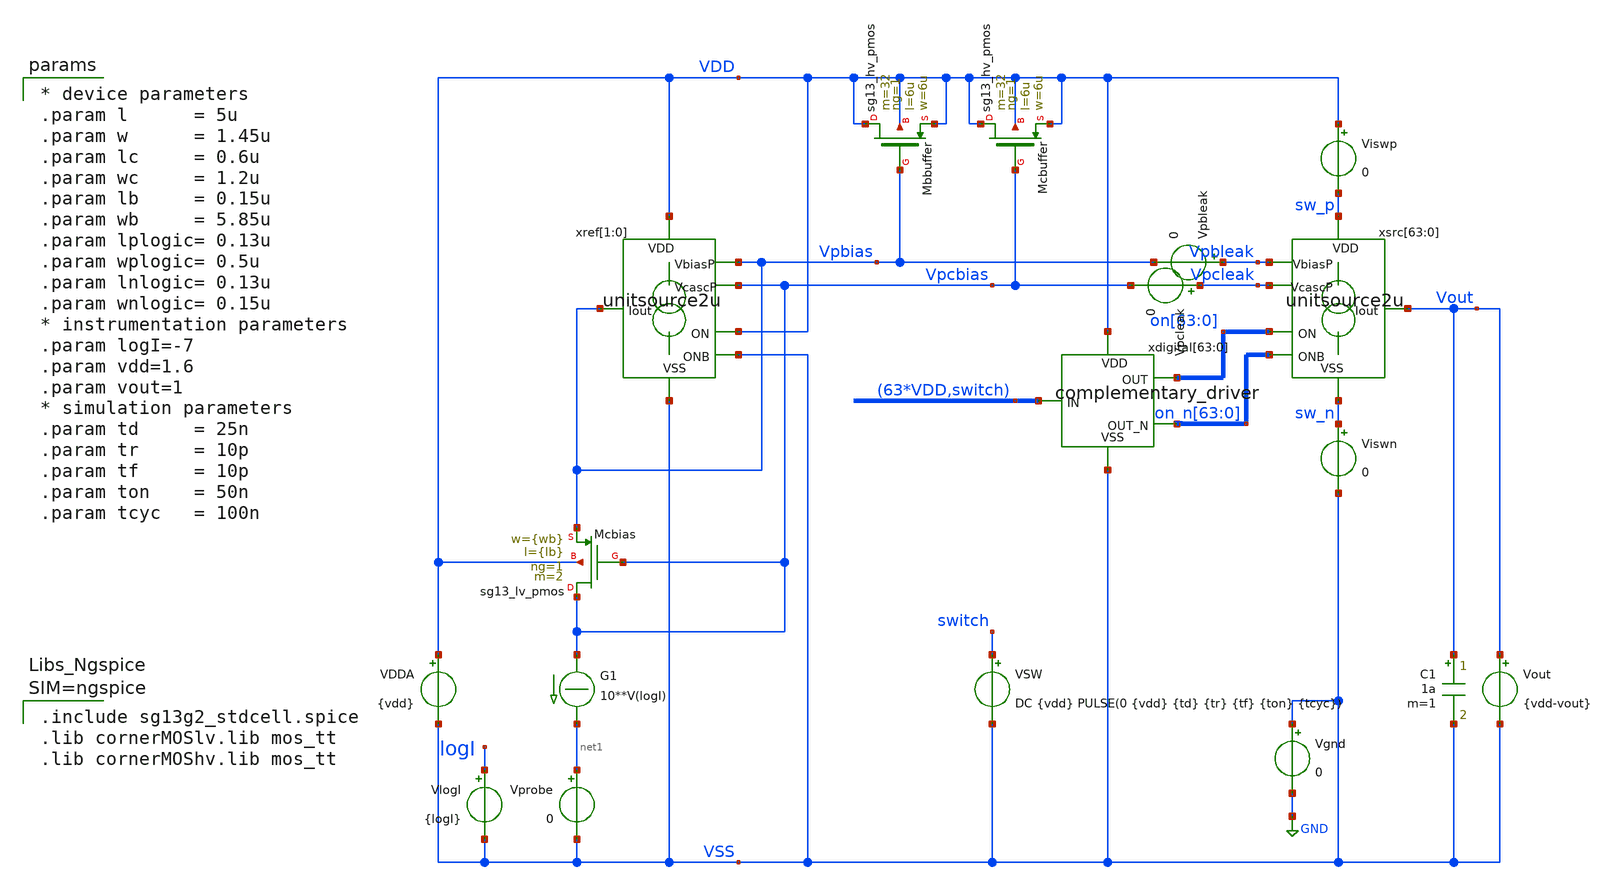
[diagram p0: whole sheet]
** sch_path: xschem/test_unitsource2u_tran.sch
**.subckt test_unitsource2u_tran
Vout Vout VSS {vdd-vout}
.save i(vout)
Vprobe net1 VSS 0
.save i(vprobe)
G1 Vpcbias net1 CUR=' 10**V(logI) '
VlogI logI VSS {logI}
.save i(vlogi)
VDDA VDD VSS {vdd}
.save i(vdda)
XMcbias Vpcbias Vpcbias Vpbias VDD sg13_lv_pmos w={wb} l={lb} ng=1 m=2 mm_ok=1
VSW switch VSS DC {vdd} PULSE(0 {vdd} {td} {tr} {tf} {ton} {tcyc})
.save i(vsw)
XMcbuffer VDD Vpcbias VDD VDD sg13_hv_pmos w=6u l=6u ng=1 m=32 mm_ok=1
XMbbuffer VDD Vpbias VDD VDD sg13_hv_pmos w=6u l=6u ng=1 m=32 mm_ok=1
xref[1] VDD Vpbias VDD VSS Vpbias Vpcbias VSS unitsource2u
xref[0] VDD Vpbias VDD VSS Vpbias Vpcbias VSS unitsource2u
xsrc[63] sw_p Vpbleak on[63] on_n[63] Vout Vpcleak sw_n unitsource2u
xsrc[62] sw_p Vpbleak on[62] on_n[62] Vout Vpcleak sw_n unitsource2u
xsrc[61] sw_p Vpbleak on[61] on_n[61] Vout Vpcleak sw_n unitsource2u
xsrc[60] sw_p Vpbleak on[60] on_n[60] Vout Vpcleak sw_n unitsource2u
xsrc[59] sw_p Vpbleak on[59] on_n[59] Vout Vpcleak sw_n unitsource2u
xsrc[58] sw_p Vpbleak on[58] on_n[58] Vout Vpcleak sw_n unitsource2u
xsrc[57] sw_p Vpbleak on[57] on_n[57] Vout Vpcleak sw_n unitsource2u
xsrc[56] sw_p Vpbleak on[56] on_n[56] Vout Vpcleak sw_n unitsource2u
xsrc[55] sw_p Vpbleak on[55] on_n[55] Vout Vpcleak sw_n unitsource2u
xsrc[54] sw_p Vpbleak on[54] on_n[54] Vout Vpcleak sw_n unitsource2u
xsrc[53] sw_p Vpbleak on[53] on_n[53] Vout Vpcleak sw_n unitsource2u
xsrc[52] sw_p Vpbleak on[52] on_n[52] Vout Vpcleak sw_n unitsource2u
xsrc[51] sw_p Vpbleak on[51] on_n[51] Vout Vpcleak sw_n unitsource2u
xsrc[50] sw_p Vpbleak on[50] on_n[50] Vout Vpcleak sw_n unitsource2u
xsrc[49] sw_p Vpbleak on[49] on_n[49] Vout Vpcleak sw_n unitsource2u
xsrc[48] sw_p Vpbleak on[48] on_n[48] Vout Vpcleak sw_n unitsource2u
xsrc[47] sw_p Vpbleak on[47] on_n[47] Vout Vpcleak sw_n unitsource2u
xsrc[46] sw_p Vpbleak on[46] on_n[46] Vout Vpcleak sw_n unitsource2u
xsrc[45] sw_p Vpbleak on[45] on_n[45] Vout Vpcleak sw_n unitsource2u
xsrc[44] sw_p Vpbleak on[44] on_n[44] Vout Vpcleak sw_n unitsource2u
xsrc[43] sw_p Vpbleak on[43] on_n[43] Vout Vpcleak sw_n unitsource2u
xsrc[42] sw_p Vpbleak on[42] on_n[42] Vout Vpcleak sw_n unitsource2u
xsrc[41] sw_p Vpbleak on[41] on_n[41] Vout Vpcleak sw_n unitsource2u
xsrc[40] sw_p Vpbleak on[40] on_n[40] Vout Vpcleak sw_n unitsource2u
xsrc[39] sw_p Vpbleak on[39] on_n[39] Vout Vpcleak sw_n unitsource2u
xsrc[38] sw_p Vpbleak on[38] on_n[38] Vout Vpcleak sw_n unitsource2u
xsrc[37] sw_p Vpbleak on[37] on_n[37] Vout Vpcleak sw_n unitsource2u
xsrc[36] sw_p Vpbleak on[36] on_n[36] Vout Vpcleak sw_n unitsource2u
xsrc[35] sw_p Vpbleak on[35] on_n[35] Vout Vpcleak sw_n unitsource2u
xsrc[34] sw_p Vpbleak on[34] on_n[34] Vout Vpcleak sw_n unitsource2u
xsrc[33] sw_p Vpbleak on[33] on_n[33] Vout Vpcleak sw_n unitsource2u
xsrc[32] sw_p Vpbleak on[32] on_n[32] Vout Vpcleak sw_n unitsource2u
xsrc[31] sw_p Vpbleak on[31] on_n[31] Vout Vpcleak sw_n unitsource2u
xsrc[30] sw_p Vpbleak on[30] on_n[30] Vout Vpcleak sw_n unitsource2u
xsrc[29] sw_p Vpbleak on[29] on_n[29] Vout Vpcleak sw_n unitsource2u
xsrc[28] sw_p Vpbleak on[28] on_n[28] Vout Vpcleak sw_n unitsource2u
xsrc[27] sw_p Vpbleak on[27] on_n[27] Vout Vpcleak sw_n unitsource2u
xsrc[26] sw_p Vpbleak on[26] on_n[26] Vout Vpcleak sw_n unitsource2u
xsrc[25] sw_p Vpbleak on[25] on_n[25] Vout Vpcleak sw_n unitsource2u
xsrc[24] sw_p Vpbleak on[24] on_n[24] Vout Vpcleak sw_n unitsource2u
xsrc[23] sw_p Vpbleak on[23] on_n[23] Vout Vpcleak sw_n unitsource2u
xsrc[22] sw_p Vpbleak on[22] on_n[22] Vout Vpcleak sw_n unitsource2u
xsrc[21] sw_p Vpbleak on[21] on_n[21] Vout Vpcleak sw_n unitsource2u
xsrc[20] sw_p Vpbleak on[20] on_n[20] Vout Vpcleak sw_n unitsource2u
xsrc[19] sw_p Vpbleak on[19] on_n[19] Vout Vpcleak sw_n unitsource2u
xsrc[18] sw_p Vpbleak on[18] on_n[18] Vout Vpcleak sw_n unitsource2u
xsrc[17] sw_p Vpbleak on[17] on_n[17] Vout Vpcleak sw_n unitsource2u
xsrc[16] sw_p Vpbleak on[16] on_n[16] Vout Vpcleak sw_n unitsource2u
xsrc[15] sw_p Vpbleak on[15] on_n[15] Vout Vpcleak sw_n unitsource2u
xsrc[14] sw_p Vpbleak on[14] on_n[14] Vout Vpcleak sw_n unitsource2u
xsrc[13] sw_p Vpbleak on[13] on_n[13] Vout Vpcleak sw_n unitsource2u
xsrc[12] sw_p Vpbleak on[12] on_n[12] Vout Vpcleak sw_n unitsource2u
xsrc[11] sw_p Vpbleak on[11] on_n[11] Vout Vpcleak sw_n unitsource2u
xsrc[10] sw_p Vpbleak on[10] on_n[10] Vout Vpcleak sw_n unitsource2u
xsrc[9] sw_p Vpbleak on[9] on_n[9] Vout Vpcleak sw_n unitsource2u
xsrc[8] sw_p Vpbleak on[8] on_n[8] Vout Vpcleak sw_n unitsource2u
xsrc[7] sw_p Vpbleak on[7] on_n[7] Vout Vpcleak sw_n unitsource2u
xsrc[6] sw_p Vpbleak on[6] on_n[6] Vout Vpcleak sw_n unitsource2u
xsrc[5] sw_p Vpbleak on[5] on_n[5] Vout Vpcleak sw_n unitsource2u
xsrc[4] sw_p Vpbleak on[4] on_n[4] Vout Vpcleak sw_n unitsource2u
xsrc[3] sw_p Vpbleak on[3] on_n[3] Vout Vpcleak sw_n unitsource2u
xsrc[2] sw_p Vpbleak on[2] on_n[2] Vout Vpcleak sw_n unitsource2u
xsrc[1] sw_p Vpbleak on[1] on_n[1] Vout Vpcleak sw_n unitsource2u
xsrc[0] sw_p Vpbleak on[0] on_n[0] Vout Vpcleak sw_n unitsource2u
Viswp VDD sw_p 0
.save i(viswp)
Viswn sw_n VSS 0
.save i(viswn)
C1 Vout VSS 1a m=1
Vgnd VSS GND 0
.save i(vgnd)
xdigital[63] VDD on[63] VDD on_n[63] VSS complementary_driver
xdigital[62] VDD on[62] VDD on_n[62] VSS complementary_driver
xdigital[61] VDD on[61] VDD on_n[61] VSS complementary_driver
xdigital[60] VDD on[60] VDD on_n[60] VSS complementary_driver
xdigital[59] VDD on[59] VDD on_n[59] VSS complementary_driver
xdigital[58] VDD on[58] VDD on_n[58] VSS complementary_driver
xdigital[57] VDD on[57] VDD on_n[57] VSS complementary_driver
xdigital[56] VDD on[56] VDD on_n[56] VSS complementary_driver
xdigital[55] VDD on[55] VDD on_n[55] VSS complementary_driver
xdigital[54] VDD on[54] VDD on_n[54] VSS complementary_driver
xdigital[53] VDD on[53] VDD on_n[53] VSS complementary_driver
xdigital[52] VDD on[52] VDD on_n[52] VSS complementary_driver
xdigital[51] VDD on[51] VDD on_n[51] VSS complementary_driver
xdigital[50] VDD on[50] VDD on_n[50] VSS complementary_driver
xdigital[49] VDD on[49] VDD on_n[49] VSS complementary_driver
xdigital[48] VDD on[48] VDD on_n[48] VSS complementary_driver
xdigital[47] VDD on[47] VDD on_n[47] VSS complementary_driver
xdigital[46] VDD on[46] VDD on_n[46] VSS complementary_driver
xdigital[45] VDD on[45] VDD on_n[45] VSS complementary_driver
xdigital[44] VDD on[44] VDD on_n[44] VSS complementary_driver
xdigital[43] VDD on[43] VDD on_n[43] VSS complementary_driver
xdigital[42] VDD on[42] VDD on_n[42] VSS complementary_driver
xdigital[41] VDD on[41] VDD on_n[41] VSS complementary_driver
xdigital[40] VDD on[40] VDD on_n[40] VSS complementary_driver
xdigital[39] VDD on[39] VDD on_n[39] VSS complementary_driver
xdigital[38] VDD on[38] VDD on_n[38] VSS complementary_driver
xdigital[37] VDD on[37] VDD on_n[37] VSS complementary_driver
xdigital[36] VDD on[36] VDD on_n[36] VSS complementary_driver
xdigital[35] VDD on[35] VDD on_n[35] VSS complementary_driver
xdigital[34] VDD on[34] VDD on_n[34] VSS complementary_driver
xdigital[33] VDD on[33] VDD on_n[33] VSS complementary_driver
xdigital[32] VDD on[32] VDD on_n[32] VSS complementary_driver
xdigital[31] VDD on[31] VDD on_n[31] VSS complementary_driver
xdigital[30] VDD on[30] VDD on_n[30] VSS complementary_driver
xdigital[29] VDD on[29] VDD on_n[29] VSS complementary_driver
xdigital[28] VDD on[28] VDD on_n[28] VSS complementary_driver
xdigital[27] VDD on[27] VDD on_n[27] VSS complementary_driver
xdigital[26] VDD on[26] VDD on_n[26] VSS complementary_driver
xdigital[25] VDD on[25] VDD on_n[25] VSS complementary_driver
xdigital[24] VDD on[24] VDD on_n[24] VSS complementary_driver
xdigital[23] VDD on[23] VDD on_n[23] VSS complementary_driver
xdigital[22] VDD on[22] VDD on_n[22] VSS complementary_driver
xdigital[21] VDD on[21] VDD on_n[21] VSS complementary_driver
xdigital[20] VDD on[20] VDD on_n[20] VSS complementary_driver
xdigital[19] VDD on[19] VDD on_n[19] VSS complementary_driver
xdigital[18] VDD on[18] VDD on_n[18] VSS complementary_driver
xdigital[17] VDD on[17] VDD on_n[17] VSS complementary_driver
xdigital[16] VDD on[16] VDD on_n[16] VSS complementary_driver
xdigital[15] VDD on[15] VDD on_n[15] VSS complementary_driver
xdigital[14] VDD on[14] VDD on_n[14] VSS complementary_driver
xdigital[13] VDD on[13] VDD on_n[13] VSS complementary_driver
xdigital[12] VDD on[12] VDD on_n[12] VSS complementary_driver
xdigital[11] VDD on[11] VDD on_n[11] VSS complementary_driver
xdigital[10] VDD on[10] VDD on_n[10] VSS complementary_driver
xdigital[9] VDD on[9] VDD on_n[9] VSS complementary_driver
xdigital[8] VDD on[8] VDD on_n[8] VSS complementary_driver
xdigital[7] VDD on[7] VDD on_n[7] VSS complementary_driver
xdigital[6] VDD on[6] VDD on_n[6] VSS complementary_driver
xdigital[5] VDD on[5] VDD on_n[5] VSS complementary_driver
xdigital[4] VDD on[4] VDD on_n[4] VSS complementary_driver
xdigital[3] VDD on[3] VDD on_n[3] VSS complementary_driver
xdigital[2] VDD on[2] VDD on_n[2] VSS complementary_driver
xdigital[1] VDD on[1] VDD on_n[1] VSS complementary_driver
xdigital[0] VDD on[0] switch on_n[0] VSS complementary_driver
Vpbleak Vpbleak Vpbias 0
.save i(vpbleak)
Vpcleak Vpcleak Vpcbias 0
.save i(vpcleak)
**** begin user architecture code


.include test_unitsource2u_tran.save
.temp=27
.options gmin=1e-15 abstol=1p method=gear
*.options savecurrents
.control
save all
op
write test_unitsource2u_tran.raw
set appendwrite
*dc Vout 0 1.6 10m VlogI -8 -6 0.5
tran 10p 200n
write test_switchedsources_tran.raw
plot title "voltages" vdd vpbias vpcbias switch "on_n[0]" "on[0]" vout
plot title "switch voltages" switch "on[0]" "on_n[0]" "xsrc.on_n[0]" "xsrc.off_n[0]" "xsrc[0].vcasc"
+ "xref[0].xsrc.drain" "xsrc[0].xsrc.drain"
*plot @n.xsw.xmbias.nsg13_lv_pmos[ids] @n.xsw.xmpullup.nsg13_lv_pmos[ids]
plot title "analog switch currents" viswp#branch-vout#branch viswn#branch
plot title "switch cross and difference currents" 0.5*(viswp#branch+viswn#branch-vout#branch)
+ viswp#branch-viswn#branch-vout#branch
plot title "gate leakage currents" vpbleak#branch vpcleak#branch
plot title "output and reference currents" vout#branch vprobe#branch
plot title "output current accuracy" 2*(vout#branch/32-vprobe#branch)/(vprobe#branch+vout#branch/32)
plot title "output current accuracy" ylimit -50m 50m
+ 2*(vout#branch/32-vprobe#branch)/(vprobe#branch+vout#branch/32)
.endc




.include sg13g2_stdcell.spice
.lib cornerMOSlv.lib mos_tt
.lib cornerMOShv.lib mos_tt



* device parameters
.param l      = 5u
.param w      = 1.45u
.param lc     = 0.6u
.param wc     = 1.2u
.param lb     = 0.15u
.param wb     = 5.85u
.param lplogic= 0.13u
.param wplogic= 0.5u
.param lnlogic= 0.13u
.param wnlogic= 0.15u
* instrumentation parameters
.param logI=-7
.param vdd=1.6
.param vout=1
* simulation parameters
.param td     = 25n
.param tr     = 10p
.param tf     = 10p
.param ton    = 50n
.param tcyc   = 100n


**** end user architecture code
**.ends

* expanding   symbol:  unitsource2u.sym # of pins=7
** sym_path: xschem/unitsource2u.sym
** sch_path: xschem/unitsource2u.sch
.subckt unitsource2u VDD VbiasP ON ONB Iout VcascP VSS
*.iopin VSS
*.iopin VDD
*.iopin VbiasP
*.iopin VcascP
*.ipin ON
*.ipin ONB
*.iopin Iout
xnonoverlap VDD VSS ON ONB on_n off_n nonoverlap
xsw VDD off_n Vcasc on_n VcascP cascodeswitch_pmos
xsrc VDD VbiasP Vcasc Iout pcsource2u
.ends


* expanding   symbol:  complementary_driver.sym # of pins=5
** sym_path: xschem/complementary_driver.sym
** sch_path: xschem/complementary_driver.sch
.subckt complementary_driver VDD OUT IN OUT_N VSS
*.iopin VSS
*.iopin VDD
*.ipin IN
*.opin OUT
*.opin OUT_N
x0 OUT_N IN VDD VSS sg13g2_inv_1
x1 OUT OUT_N VDD VSS sg13g2_inv_1
.ends


* expanding   symbol:  nonoverlap.sym # of pins=6
** sym_path: xschem/nonoverlap.sym
** sch_path: xschem/nonoverlap.sch
.subckt nonoverlap VDD VSS INP INN OUTN OUTP
*.iopin VSS
*.iopin VDD
*.ipin INP
*.ipin INN
*.opin OUTP
*.opin OUTN
XM1 OUTN INP VDD VDD sg13_lv_pmos w=0.3u l=0.13u ng=1 m=1 mm_ok=1
XM2 OUTP INN VDD VDD sg13_lv_pmos w=0.3u l=0.13u ng=1 m=1 mm_ok=1
XM3 OUTN OUTP VSS VSS sg13_lv_nmos w=0.15u l=0.52u ng=1 m=1 mm_ok=1
XM4 OUTP OUTN VSS VSS sg13_lv_nmos w=0.15u l=0.52u ng=1 m=1 mm_ok=1
.ends


* expanding   symbol:  cascodeswitch_pmos.sym # of pins=5
** sym_path: xschem/cascodeswitch_pmos.sym
** sch_path: xschem/cascodeswitch_pmos.sch
.subckt cascodeswitch_pmos VDD off_n Vcasc on_n Vbpcasc
*.ipin off_n
*.ipin Vbpcasc
*.opin Vcasc
*.ipin on_n
*.ipin VDD
XMpullup Vcasc off_n VDD VDD sg13_lv_pmos w=0.3u l=0.13u ng=1 m=1 mm_ok=1
XMbias Vbpcasc on_n Vcasc VDD sg13_lv_pmos w=0.3u l=0.13u ng=1 m=1 mm_ok=1
.ends


* expanding   symbol:  pcsource2u.sym # of pins=4
** sym_path: xschem/pcsource2u.sym
** sch_path: xschem/pcsource2u.sch
.subckt pcsource2u VDD VbiasP VcascodeP Iout
*.ipin VcascodeP
*.ipin VbiasP
*.opin Iout
*.ipin VDD
XMsrc drain net4 VDD net1 sg13_lv_pmos w=1.45u l=5u ng=1 m=1 mm_ok=1
XMcasc Iout net3 drain net2 sg13_lv_pmos w=1.2u l=0.6u ng=1 m=1 mm_ok=1
Vgsrc net4 VbiasP 0
.save i(vgsrc)
Vgcasc net3 VcascodeP 0
.save i(vgcasc)
Vbsrc VDD net1 0
.save i(vbsrc)
Vbcasc VDD net2 0
.save i(vbcasc)
.ends


* expanding   symbol:  sg13g2_stdcells/sg13g2_inv_1.sym # of pins=2
** sym_path: sg13g2_stdcells/sg13g2_inv_1.sym
** sch_path: sg13g2_stdcells/sg13g2_inv_1.sch
.subckt sg13g2_inv_1 Y A VDD VSS
*.opin Y
*.ipin A
*.iopin VDD
*.iopin VSS
XM1 Y A VSS VSS sg13_lv_nmos w=740.00n l=130.00n ng=1 m=1 mm_ok=1
XM2 Y A VDD VDD sg13_lv_pmos w=1.12u l=130.00n ng=1 m=1 mm_ok=1
.ends

.GLOBAL GND
.end
